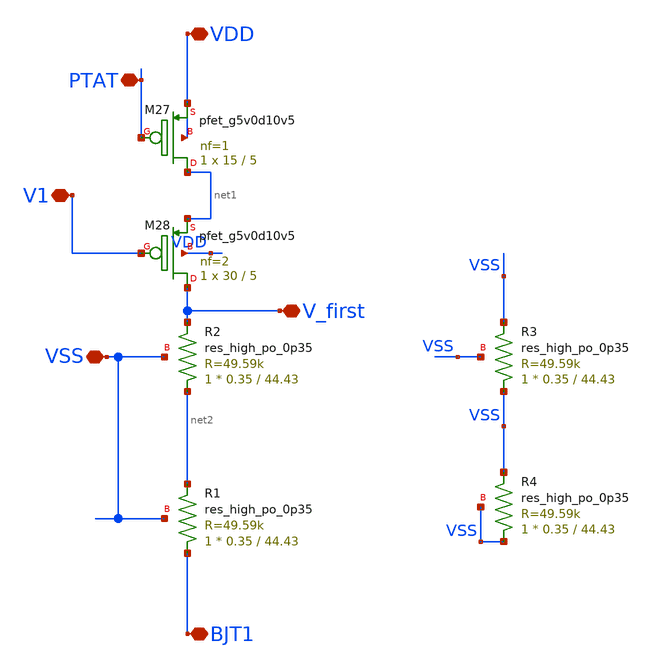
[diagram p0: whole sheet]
** sch_path: xschem/xschem_BGR_Top/CTAT.sch
**.subckt CTAT VDD PTAT V1 BJT1 V_first VSS
*.iopin VDD
*.iopin PTAT
*.iopin V1
*.iopin BJT1
*.iopin V_first
*.iopin VSS
XM27 net1 PTAT VDD VDD sky130_fd_pr__pfet_g5v0d10v5 L=5 W=15 nf=1 ad='int((nf+1)/2) * W/nf * 0.29' as='int((nf+2)/2) * W/nf * 0.29'
+ pd='2*int((nf+1)/2) * (W/nf + 0.29)' ps='2*int((nf+2)/2) * (W/nf + 0.29)' nrd='0.29 / W' nrs='0.29 / W'
+ sa=0 sb=0 sd=0 mult=1 m=1
XM28 V_first V1 net1 VDD sky130_fd_pr__pfet_g5v0d10v5 L=5 W=30 nf=2 ad='int((nf+1)/2) * W/nf * 0.29'
+ as='int((nf+2)/2) * W/nf * 0.29' pd='2*int((nf+1)/2) * (W/nf + 0.29)' ps='2*int((nf+2)/2) * (W/nf + 0.29)'
+ nrd='0.29 / W' nrs='0.29 / W' sa=0 sb=0 sd=0 mult=1 m=1
XR2 net2 V_first VSS sky130_fd_pr__res_high_po_0p35 L=44.43 mult=1 m=1
XR1 BJT1 net2 VSS sky130_fd_pr__res_high_po_0p35 L=44.43 mult=1 m=1
XR3 VSS VSS VSS sky130_fd_pr__res_high_po_0p35 L=44.43 mult=1 m=1
XR4 VSS VSS VSS sky130_fd_pr__res_high_po_0p35 L=44.43 mult=1 m=1
**.ends
.end
